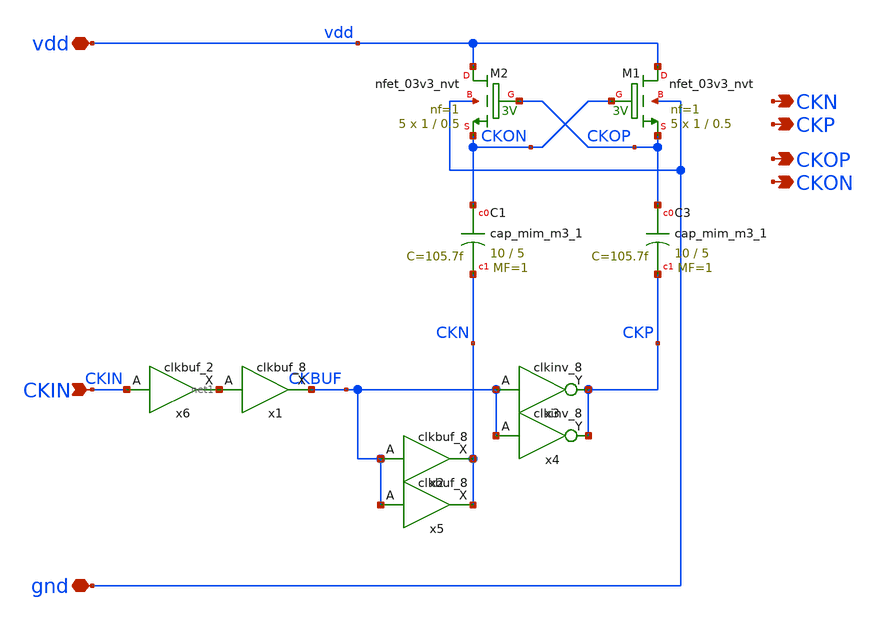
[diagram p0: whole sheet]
** sch_path: xschem/snh_clock_driver.sch
**.subckt snh_clock_driver vdd gnd CKIN CKN CKP CKOP CKON
*.iopin vdd
*.iopin gnd
*.ipin CKIN
*.opin CKN
*.opin CKP
*.opin CKOP
*.opin CKON
XC1 CKON CKN sky130_fd_pr__cap_mim_m3_1 W=10 L=5 MF=1 m=1
XC3 CKOP CKP sky130_fd_pr__cap_mim_m3_1 W=10 L=5 MF=1 m=1
x3 CKBUF gnd gnd vdd vdd CKP sky130_fd_sc_hd__clkinv_8
x2 CKBUF gnd gnd vdd vdd CKN sky130_fd_sc_hd__clkbuf_8
x1 net1 gnd gnd vdd vdd CKBUF sky130_fd_sc_hd__clkbuf_8
XM2 vdd CKOP CKON gnd sky130_fd_pr__nfet_03v3_nvt L=0.5 W=1 nf=1 ad='int((nf+1)/2) * W/nf * 0.29' as='int((nf+2)/2) * W/nf * 0.29'
+ pd='2*int((nf+1)/2) * (W/nf + 0.29)' ps='2*int((nf+2)/2) * (W/nf + 0.29)' nrd='0.29 / W' nrs='0.29 / W'
+ sa=0 sb=0 sd=0 mult=5 m=5
x4 CKBUF gnd gnd vdd vdd CKP sky130_fd_sc_hd__clkinv_8
x5 CKBUF gnd gnd vdd vdd CKN sky130_fd_sc_hd__clkbuf_8
x6 CKIN gnd gnd vdd vdd net1 sky130_fd_sc_hd__clkbuf_2
XM1 vdd CKON CKOP gnd sky130_fd_pr__nfet_03v3_nvt L=0.5 W=1 nf=1 ad='int((nf+1)/2) * W/nf * 0.29' as='int((nf+2)/2) * W/nf * 0.29'
+ pd='2*int((nf+1)/2) * (W/nf + 0.29)' ps='2*int((nf+2)/2) * (W/nf + 0.29)' nrd='0.29 / W' nrs='0.29 / W'
+ sa=0 sb=0 sd=0 mult=5 m=5
**.ends
.end
